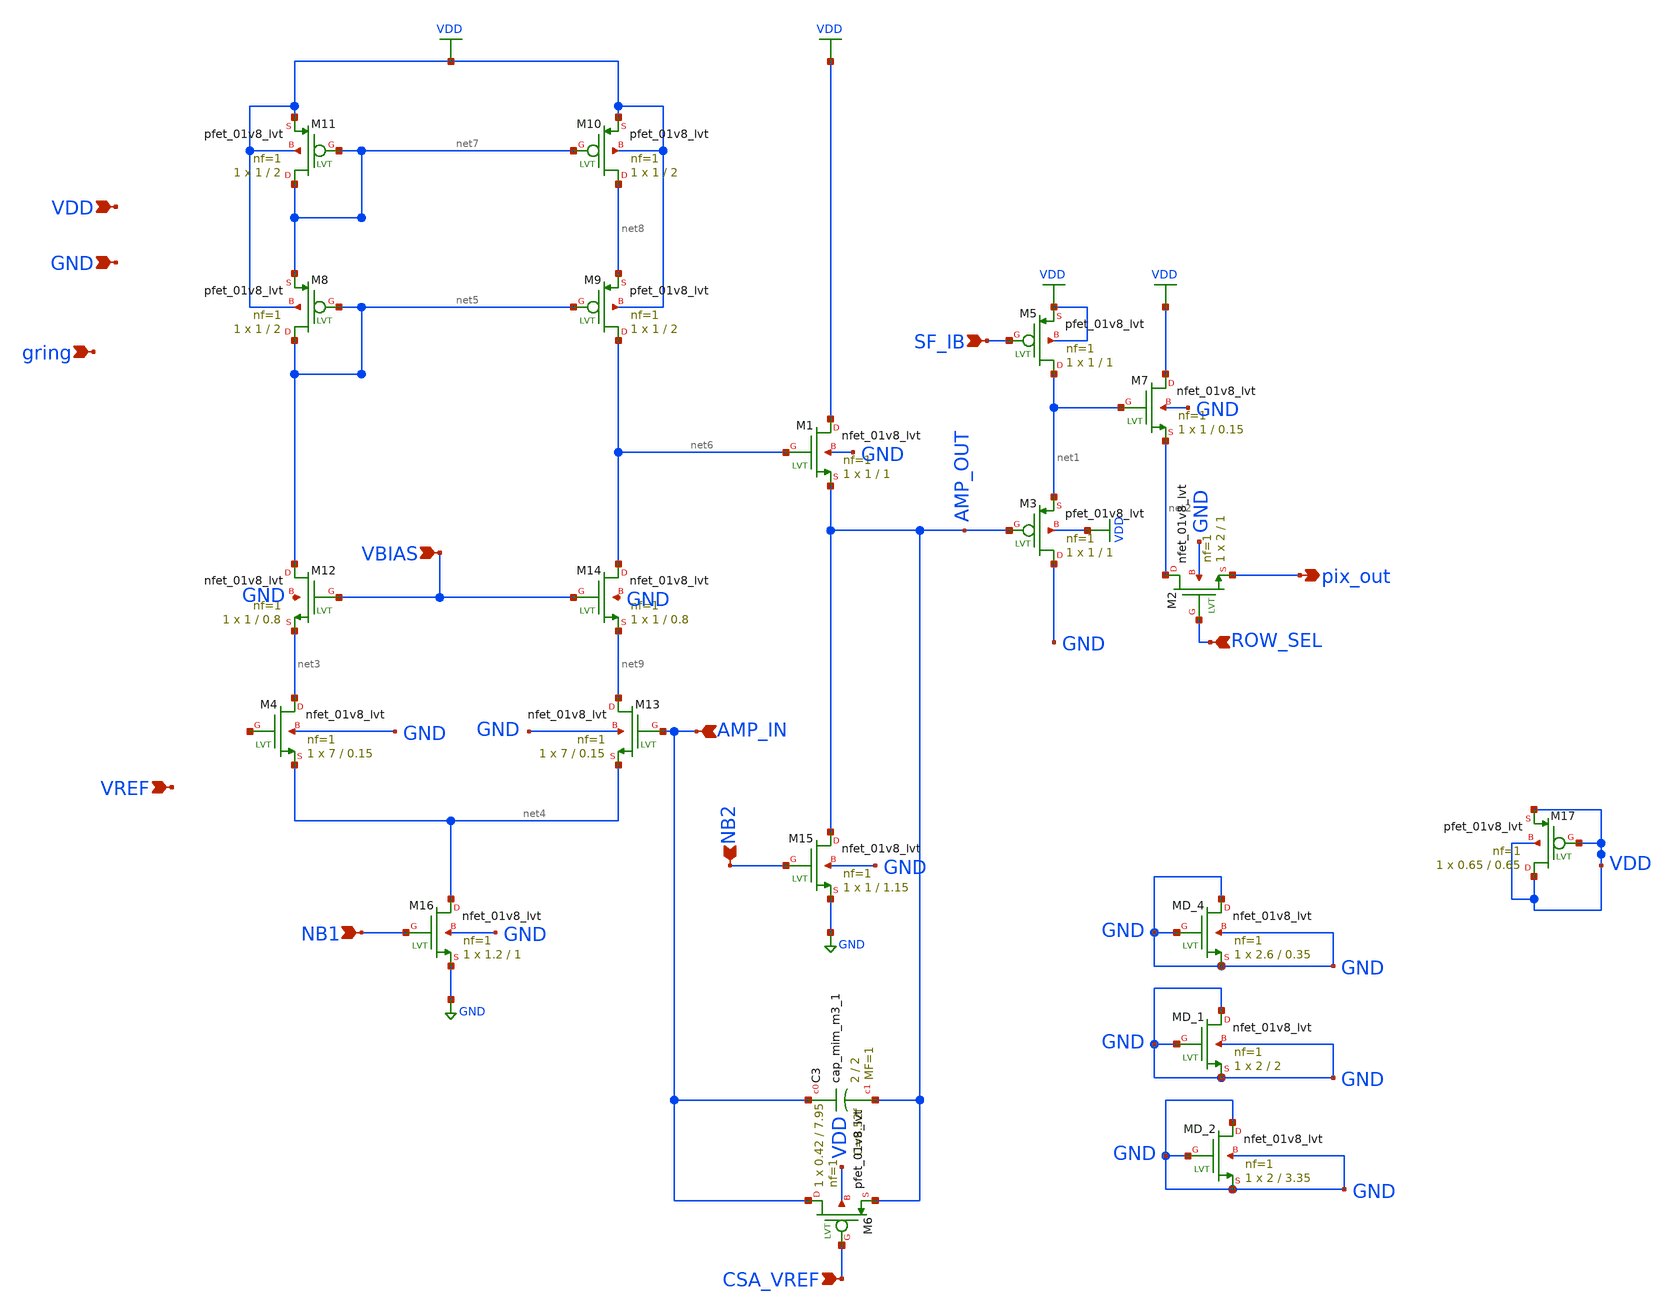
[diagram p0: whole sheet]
** sch_path: xschem/marker_pixel.sch
**.subckt marker_pixel pix_out SF_IB ROW_SEL VREF AMP_IN NB1 CSA_VREF VBIAS NB2 VDD GND gring
*.opin pix_out
*.ipin SF_IB
*.ipin ROW_SEL
*.ipin VREF
*.ipin AMP_IN
*.ipin NB1
*.ipin CSA_VREF
*.ipin VBIAS
*.ipin NB2
*.ipin VDD
*.ipin GND
*.ipin gring
XM2 net2 ROW_SEL pix_out GND sky130_fd_pr__nfet_01v8_lvt L=1 W=2 nf=1 ad='int((nf+1)/2) * W/nf * 0.29'
+ as='int((nf+2)/2) * W/nf * 0.29' pd='2*int((nf+1)/2) * (W/nf + 0.29)' ps='2*int((nf+2)/2) * (W/nf + 0.29)'
+ nrd='0.29 / W' nrs='0.29 / W' sa=0 sb=0 sd=0 mult=1 m=1
XM3 GND AMP_OUT net1 VDD sky130_fd_pr__pfet_01v8_lvt L=1 W=1 nf=1 ad='int((nf+1)/2) * W/nf * 0.29' as='int((nf+2)/2) * W/nf * 0.29'
+ pd='2*int((nf+1)/2) * (W/nf + 0.29)' ps='2*int((nf+2)/2) * (W/nf + 0.29)' nrd='0.29 / W' nrs='0.29 / W'
+ sa=0 sb=0 sd=0 mult=1 m=1
XM5 net1 SF_IB VDD VDD sky130_fd_pr__pfet_01v8_lvt L=1 W=1 nf=1 ad='int((nf+1)/2) * W/nf * 0.29' as='int((nf+2)/2) * W/nf * 0.29'
+ pd='2*int((nf+1)/2) * (W/nf + 0.29)' ps='2*int((nf+2)/2) * (W/nf + 0.29)' nrd='0.29 / W' nrs='0.29 / W'
+ sa=0 sb=0 sd=0 mult=1 m=1
XM7 VDD net1 net2 GND sky130_fd_pr__nfet_01v8_lvt L=0.15 W=1 nf=1 ad='int((nf+1)/2) * W/nf * 0.29' as='int((nf+2)/2) * W/nf * 0.29'
+ pd='2*int((nf+1)/2) * (W/nf + 0.29)' ps='2*int((nf+2)/2) * (W/nf + 0.29)' nrd='0.29 / W' nrs='0.29 / W'
+ sa=0 sb=0 sd=0 mult=1 m=1
XM1 VDD net6 AMP_OUT GND sky130_fd_pr__nfet_01v8_lvt L=1 W=1 nf=1 ad='int((nf+1)/2) * W/nf * 0.29' as='int((nf+2)/2) * W/nf * 0.29'
+ pd='2*int((nf+1)/2) * (W/nf + 0.29)' ps='2*int((nf+2)/2) * (W/nf + 0.29)' nrd='0.29 / W' nrs='0.29 / W'
+ sa=0 sb=0 sd=0 mult=1 m=1
XM8 net5 net5 net7 VDD sky130_fd_pr__pfet_01v8_lvt L=2 W=1 nf=1 ad='int((nf+1)/2) * W/nf * 0.29' as='int((nf+2)/2) * W/nf * 0.29'
+ pd='2*int((nf+1)/2) * (W/nf + 0.29)' ps='2*int((nf+2)/2) * (W/nf + 0.29)' nrd='0.29 / W' nrs='0.29 / W'
+ sa=0 sb=0 sd=0 mult=1 m=1
XM10 net8 net7 VDD VDD sky130_fd_pr__pfet_01v8_lvt L=2 W=1 nf=1 ad='int((nf+1)/2) * W/nf * 0.29' as='int((nf+2)/2) * W/nf * 0.29'
+ pd='2*int((nf+1)/2) * (W/nf + 0.29)' ps='2*int((nf+2)/2) * (W/nf + 0.29)' nrd='0.29 / W' nrs='0.29 / W'
+ sa=0 sb=0 sd=0 mult=1 m=1
XM11 net7 net7 VDD VDD sky130_fd_pr__pfet_01v8_lvt L=2 W=1 nf=1 ad='int((nf+1)/2) * W/nf * 0.29' as='int((nf+2)/2) * W/nf * 0.29'
+ pd='2*int((nf+1)/2) * (W/nf + 0.29)' ps='2*int((nf+2)/2) * (W/nf + 0.29)' nrd='0.29 / W' nrs='0.29 / W'
+ sa=0 sb=0 sd=0 mult=1 m=1
XM15 AMP_OUT NB2 GND GND sky130_fd_pr__nfet_01v8_lvt L=1.15 W=1 nf=1 ad='int((nf+1)/2) * W/nf * 0.29'
+ as='int((nf+2)/2) * W/nf * 0.29' pd='2*int((nf+1)/2) * (W/nf + 0.29)' ps='2*int((nf+2)/2) * (W/nf + 0.29)'
+ nrd='0.29 / W' nrs='0.29 / W' sa=0 sb=0 sd=0 mult=1 m=1
XM16 net4 NB1 GND GND sky130_fd_pr__nfet_01v8_lvt L=1 W=1.2 nf=1 ad='int((nf+1)/2) * W/nf * 0.29' as='int((nf+2)/2) * W/nf * 0.29'
+ pd='2*int((nf+1)/2) * (W/nf + 0.29)' ps='2*int((nf+2)/2) * (W/nf + 0.29)' nrd='0.29 / W' nrs='0.29 / W'
+ sa=0 sb=0 sd=0 mult=1 m=1
XC3 AMP_IN AMP_OUT sky130_fd_pr__cap_mim_m3_1 W=2 L=2 MF=1 m=1
XM4 net3 net10 net4 GND sky130_fd_pr__nfet_01v8_lvt L=0.15 W=7 nf=1 ad='int((nf+1)/2) * W/nf * 0.29'
+ as='int((nf+2)/2) * W/nf * 0.29' pd='2*int((nf+1)/2) * (W/nf + 0.29)' ps='2*int((nf+2)/2) * (W/nf + 0.29)'
+ nrd='0.29 / W' nrs='0.29 / W' sa=0 sb=0 sd=0 mult=1 m=1
XM6 AMP_IN CSA_VREF AMP_OUT VDD sky130_fd_pr__pfet_01v8_lvt L=7.95 W=0.42 nf=1 ad='int((nf+1)/2) * W/nf * 0.29'
+ as='int((nf+2)/2) * W/nf * 0.29' pd='2*int((nf+1)/2) * (W/nf + 0.29)' ps='2*int((nf+2)/2) * (W/nf + 0.29)'
+ nrd='0.29 / W' nrs='0.29 / W' sa=0 sb=0 sd=0 mult=1 m=1
XM9 net6 net5 net8 VDD sky130_fd_pr__pfet_01v8_lvt L=2 W=1 nf=1 ad='int((nf+1)/2) * W/nf * 0.29' as='int((nf+2)/2) * W/nf * 0.29'
+ pd='2*int((nf+1)/2) * (W/nf + 0.29)' ps='2*int((nf+2)/2) * (W/nf + 0.29)' nrd='0.29 / W' nrs='0.29 / W'
+ sa=0 sb=0 sd=0 mult=1 m=1
XM12 net5 VBIAS net3 GND sky130_fd_pr__nfet_01v8_lvt L=0.8 W=1 nf=1 ad='int((nf+1)/2) * W/nf * 0.29'
+ as='int((nf+2)/2) * W/nf * 0.29' pd='2*int((nf+1)/2) * (W/nf + 0.29)' ps='2*int((nf+2)/2) * (W/nf + 0.29)'
+ nrd='0.29 / W' nrs='0.29 / W' sa=0 sb=0 sd=0 mult=1 m=1
XM13 net9 AMP_IN net4 GND sky130_fd_pr__nfet_01v8_lvt L=0.15 W=7 nf=1 ad='int((nf+1)/2) * W/nf * 0.29'
+ as='int((nf+2)/2) * W/nf * 0.29' pd='2*int((nf+1)/2) * (W/nf + 0.29)' ps='2*int((nf+2)/2) * (W/nf + 0.29)'
+ nrd='0.29 / W' nrs='0.29 / W' sa=0 sb=0 sd=0 mult=1 m=1
XM14 net6 VBIAS net9 GND sky130_fd_pr__nfet_01v8_lvt L=0.8 W=1 nf=1 ad='int((nf+1)/2) * W/nf * 0.29'
+ as='int((nf+2)/2) * W/nf * 0.29' pd='2*int((nf+1)/2) * (W/nf + 0.29)' ps='2*int((nf+2)/2) * (W/nf + 0.29)'
+ nrd='0.29 / W' nrs='0.29 / W' sa=0 sb=0 sd=0 mult=1 m=1
XMD_4 GND GND GND GND sky130_fd_pr__nfet_01v8_lvt L=0.35 W=2.6 nf=1 ad='int((nf+1)/2) * W/nf * 0.29'
+ as='int((nf+2)/2) * W/nf * 0.29' pd='2*int((nf+1)/2) * (W/nf + 0.29)' ps='2*int((nf+2)/2) * (W/nf + 0.29)'
+ nrd='0.29 / W' nrs='0.29 / W' sa=0 sb=0 sd=0 mult=1 m=1
XMD_1 GND GND GND GND sky130_fd_pr__nfet_01v8_lvt L=2 W=2 nf=1 ad='int((nf+1)/2) * W/nf * 0.29' as='int((nf+2)/2) * W/nf * 0.29'
+ pd='2*int((nf+1)/2) * (W/nf + 0.29)' ps='2*int((nf+2)/2) * (W/nf + 0.29)' nrd='0.29 / W' nrs='0.29 / W'
+ sa=0 sb=0 sd=0 mult=1 m=1
XM17 VDD VDD VDD VDD sky130_fd_pr__pfet_01v8_lvt L=0.65 W=0.65 nf=1 ad='int((nf+1)/2) * W/nf * 0.29'
+ as='int((nf+2)/2) * W/nf * 0.29' pd='2*int((nf+1)/2) * (W/nf + 0.29)' ps='2*int((nf+2)/2) * (W/nf + 0.29)'
+ nrd='0.29 / W' nrs='0.29 / W' sa=0 sb=0 sd=0 mult=1 m=1
XMD_2 GND GND GND GND sky130_fd_pr__nfet_01v8_lvt L=3.35 W=2 nf=1 ad='int((nf+1)/2) * W/nf * 0.29' as='int((nf+2)/2) * W/nf * 0.29'
+ pd='2*int((nf+1)/2) * (W/nf + 0.29)' ps='2*int((nf+2)/2) * (W/nf + 0.29)' nrd='0.29 / W' nrs='0.29 / W'
+ sa=0 sb=0 sd=0 mult=1 m=1
**.ends
.GLOBAL VDD
.GLOBAL GND
.end
